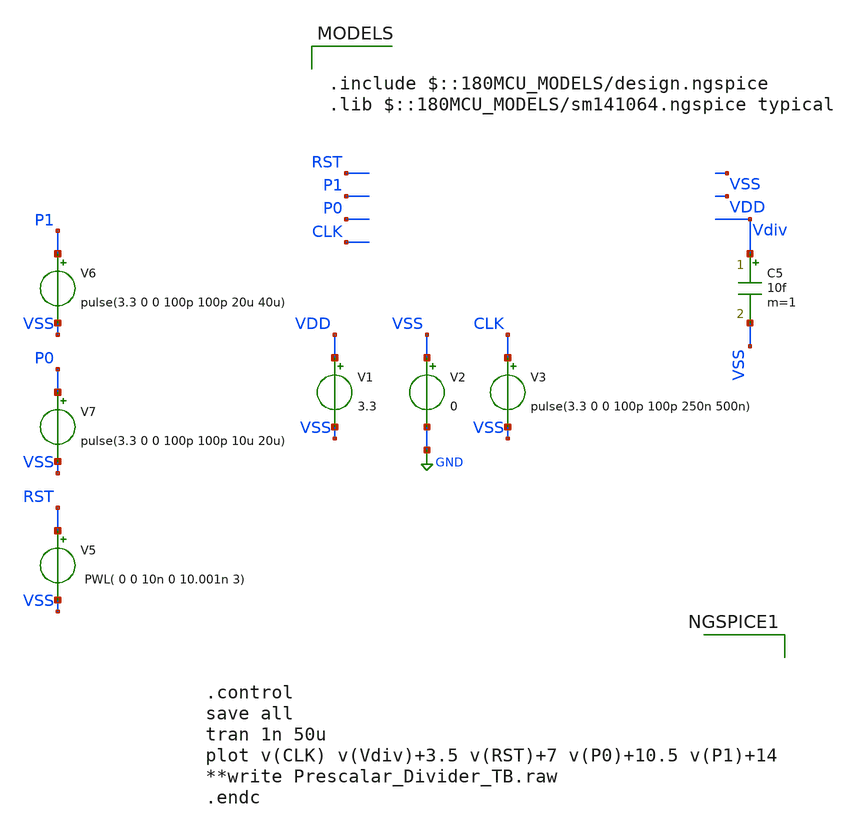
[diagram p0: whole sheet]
** sch_path: Clock_Generator_PAKISTAN_02/xschem/Prescalar_Divider_TB.sch
**.subckt Prescalar_Divider_TB
V1 VDD VSS 3.3
V2 VSS GND 0
V3 CLK VSS pulse(3.3 0 0 100p 100p 250n 500n)
C5 Vdiv VSS 10f m=1
V5 RST VSS PWL( 0 0 10n 0 10.001n 3)
V6 P1 VSS pulse(3.3 0 0 100p 100p 20u 40u)
V7 P0 VSS pulse(3.3 0 0 100p 100p 10u 20u)
**** begin user architecture code

.include $::180MCU_MODELS/design.ngspice
.lib $::180MCU_MODELS/sm141064.ngspice typical




.control
save all
tran 1n 50u
plot v(CLK) v(Vdiv)+3.5 v(RST)+7 v(P0)+10.5 v(P1)+14
**write Prescalar_Divider_TB.raw
.endc


**** end user architecture code
**.ends
.GLOBAL GND
.end
